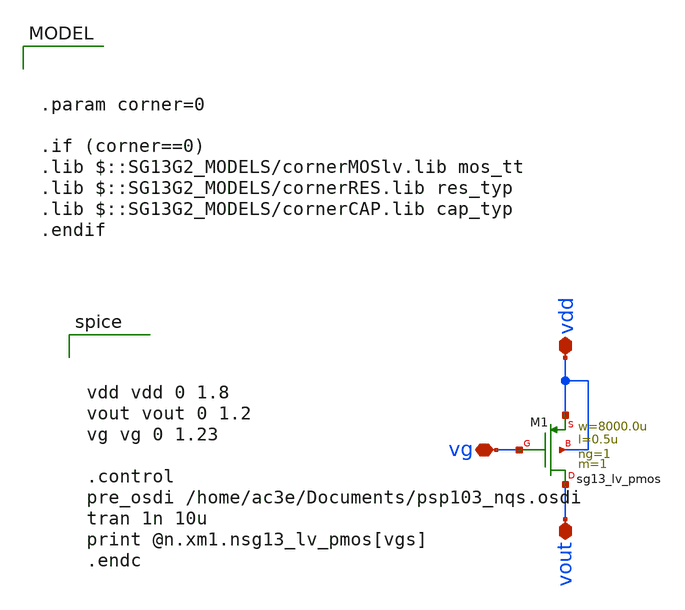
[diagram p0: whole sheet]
** sch_path: xschem/pt.sch
**.subckt pt vdd vout vg
*.iopin vdd
*.iopin vout
*.iopin vg
XM1 vout vg vdd vdd sg13_lv_pmos w=8000.0u l=0.5u ng=1 m=1 mm_ok=1
**** begin user architecture code



vdd vdd 0 1.8
vout vout 0 1.2
vg vg 0 1.23

.control
pre_osdi /home/ac3e/Documents/psp103_nqs.osdi
tran 1n 10u
print @n.xm1.nsg13_lv_pmos[vgs]
.endc





.param corner=0

.if (corner==0)
.lib $::SG13G2_MODELS/cornerMOSlv.lib mos_tt
.lib $::SG13G2_MODELS/cornerRES.lib res_typ
.lib $::SG13G2_MODELS/cornerCAP.lib cap_typ
.endif

**** end user architecture code
**.ends
.end
